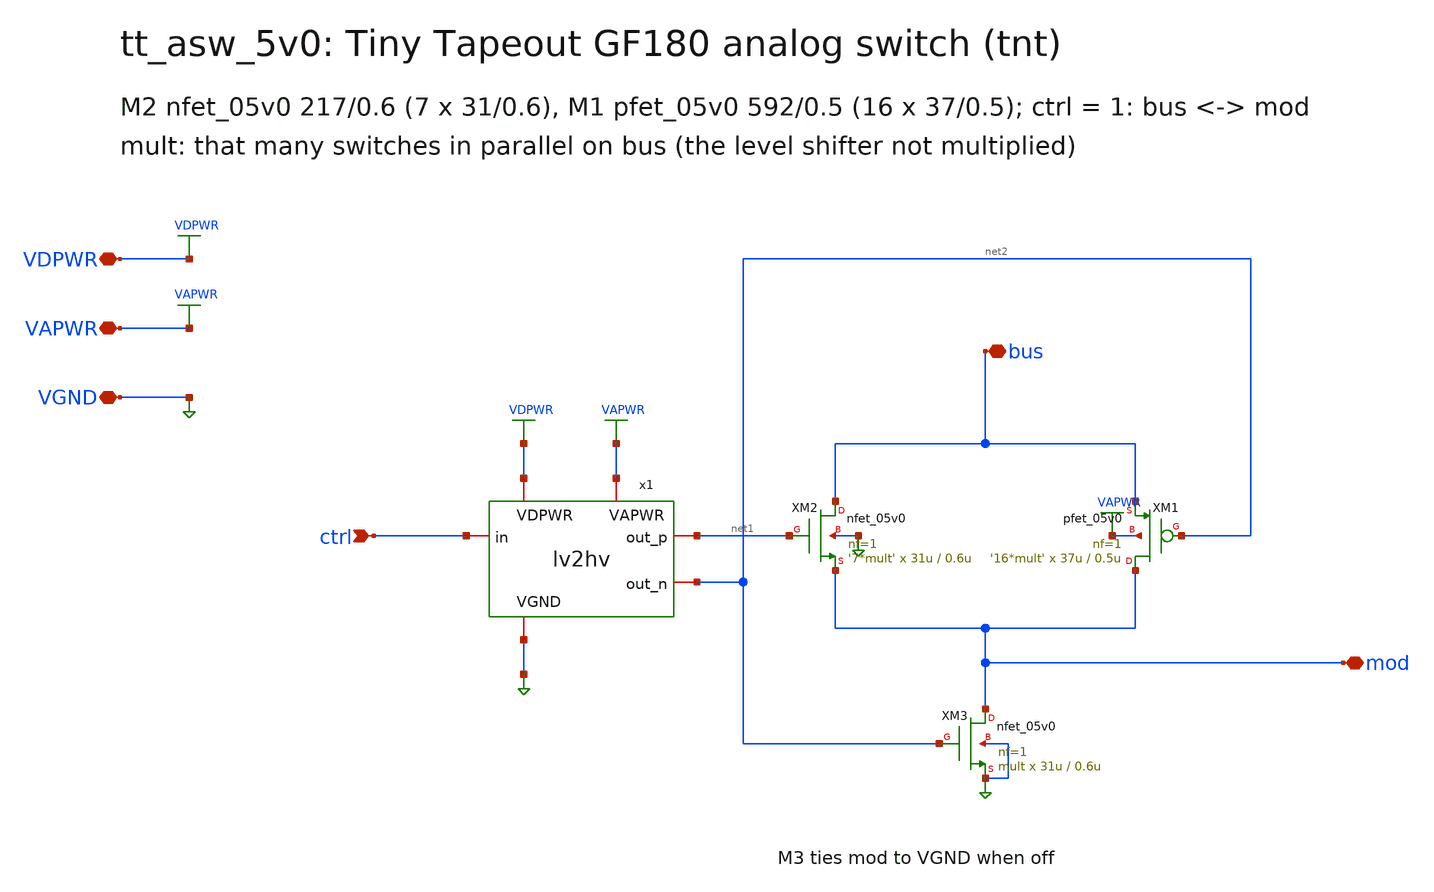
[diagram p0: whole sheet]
** sch_path: xschem/tt_asw_5v0.sch
**.subckt tt_asw_5v0 VGND VDPWR VAPWR ctrl mod bus
*.iopin VGND
*.iopin VDPWR
*.iopin VAPWR
*.ipin ctrl
*.iopin mod
*.iopin bus
x1 VGND VDPWR VAPWR ctrl net1 net2 lv2hv
XM2 bus net1 mod VGND nfet_05v0 L=0.6u W=31u nf=1 ad=3.189p as=3.189p pd=35.63u ps=35.63u nrd=0 nrs=0
+ sa=0 sb=0 sd=0 m='7*mult'
XM1 mod net2 bus VAPWR pfet_05v0 L=0.5u W=37u nf=1 ad=3.330p as=3.746p pd=37.18u ps=41.83u nrd=0 nrs=0
+ sa=0 sb=0 sd=0 m='16*mult'
XM3 mod net2 VGND VGND nfet_05v0 L=0.6u W=31u nf=1 ad=5.58p as=5.58p pd=62.36u ps=62.36u nrd=0 nrs=0
+ sa=0 sb=0 sd=0 m=mult
**.ends

* expanding   symbol:  lv2hv.sym # of pins=6
** sym_path: xschem/lv2hv.sym
** sch_path: xschem/lv2hv.sch
.subckt lv2hv VGND VDPWR VAPWR in out_p out_n
*.iopin VGND
*.iopin VDPWR
*.iopin VAPWR
*.ipin in
*.opin out_p
*.opin out_n
XM1 net1 in VDPWR VDPWR pfet_03v3 L=0.28u W=2.0u nf=1 ad=0.36p as=0.36p pd=4.36u ps=4.36u nrd=0
+ nrs=0 sa=0 sb=0 sd=0 m=1
XM2 net1 in VGND VGND nfet_03v3 L=0.28u W=0.89u nf=1 ad=0.1602p as=0.1602p pd=2.14u ps=2.14u nrd=0
+ nrs=0 sa=0 sb=0 sd=0 m=1
XM3 net2 net1 VDPWR VDPWR pfet_03v3 L=0.28u W=2.0u nf=1 ad=0.36p as=0.36p pd=4.36u ps=4.36u nrd=0
+ nrs=0 sa=0 sb=0 sd=0 m=1
XM4 net2 net1 VGND VGND nfet_03v3 L=0.28u W=0.89u nf=1 ad=0.1602p as=0.1602p pd=2.14u ps=2.14u nrd=0
+ nrs=0 sa=0 sb=0 sd=0 m=1
XM5 net3 net4 VAPWR VAPWR pfet_05v0 L=0.5u W=0.5u nf=1 ad=0.09p as=0.09p pd=1.36u ps=1.36u nrd=0
+ nrs=0 sa=0 sb=0 sd=0 m=1
XM6 net3 net2 VGND VGND nfet_05v0 L=0.6u W=0.5u nf=1 ad=0.09p as=0.09p pd=1.36u ps=1.36u nrd=0 nrs=0
+ sa=0 sb=0 sd=0 m=1
XM7 net4 net3 VAPWR VAPWR pfet_05v0 L=0.5u W=0.5u nf=1 ad=0.09p as=0.09p pd=1.36u ps=1.36u nrd=0
+ nrs=0 sa=0 sb=0 sd=0 m=1
XM8 net4 net1 VGND VGND nfet_05v0 L=0.6u W=0.5u nf=1 ad=0.09p as=0.09p pd=1.36u ps=1.36u nrd=0 nrs=0
+ sa=0 sb=0 sd=0 m=1
XM9 out_p net3 VAPWR VAPWR pfet_05v0 L=0.5u W=1.0u nf=2 ad=0.09p as=0.18p pd=1.36u ps=2.72u nrd=0
+ nrs=0 sa=0 sb=0 sd=0 m=1
XM10 out_p net3 VGND VGND nfet_05v0 L=0.6u W=0.5u nf=1 ad=0.09p as=0.09p pd=1.36u ps=1.36u nrd=0
+ nrs=0 sa=0 sb=0 sd=0 m=1
XM11 out_n net4 VAPWR VAPWR pfet_05v0 L=0.5u W=1.0u nf=2 ad=0.09p as=0.18p pd=1.36u ps=2.72u nrd=0
+ nrs=0 sa=0 sb=0 sd=0 m=1
XM12 out_n net4 VGND VGND nfet_05v0 L=0.6u W=0.5u nf=1 ad=0.09p as=0.09p pd=1.36u ps=1.36u nrd=0
+ nrs=0 sa=0 sb=0 sd=0 m=1
.ends

.end
